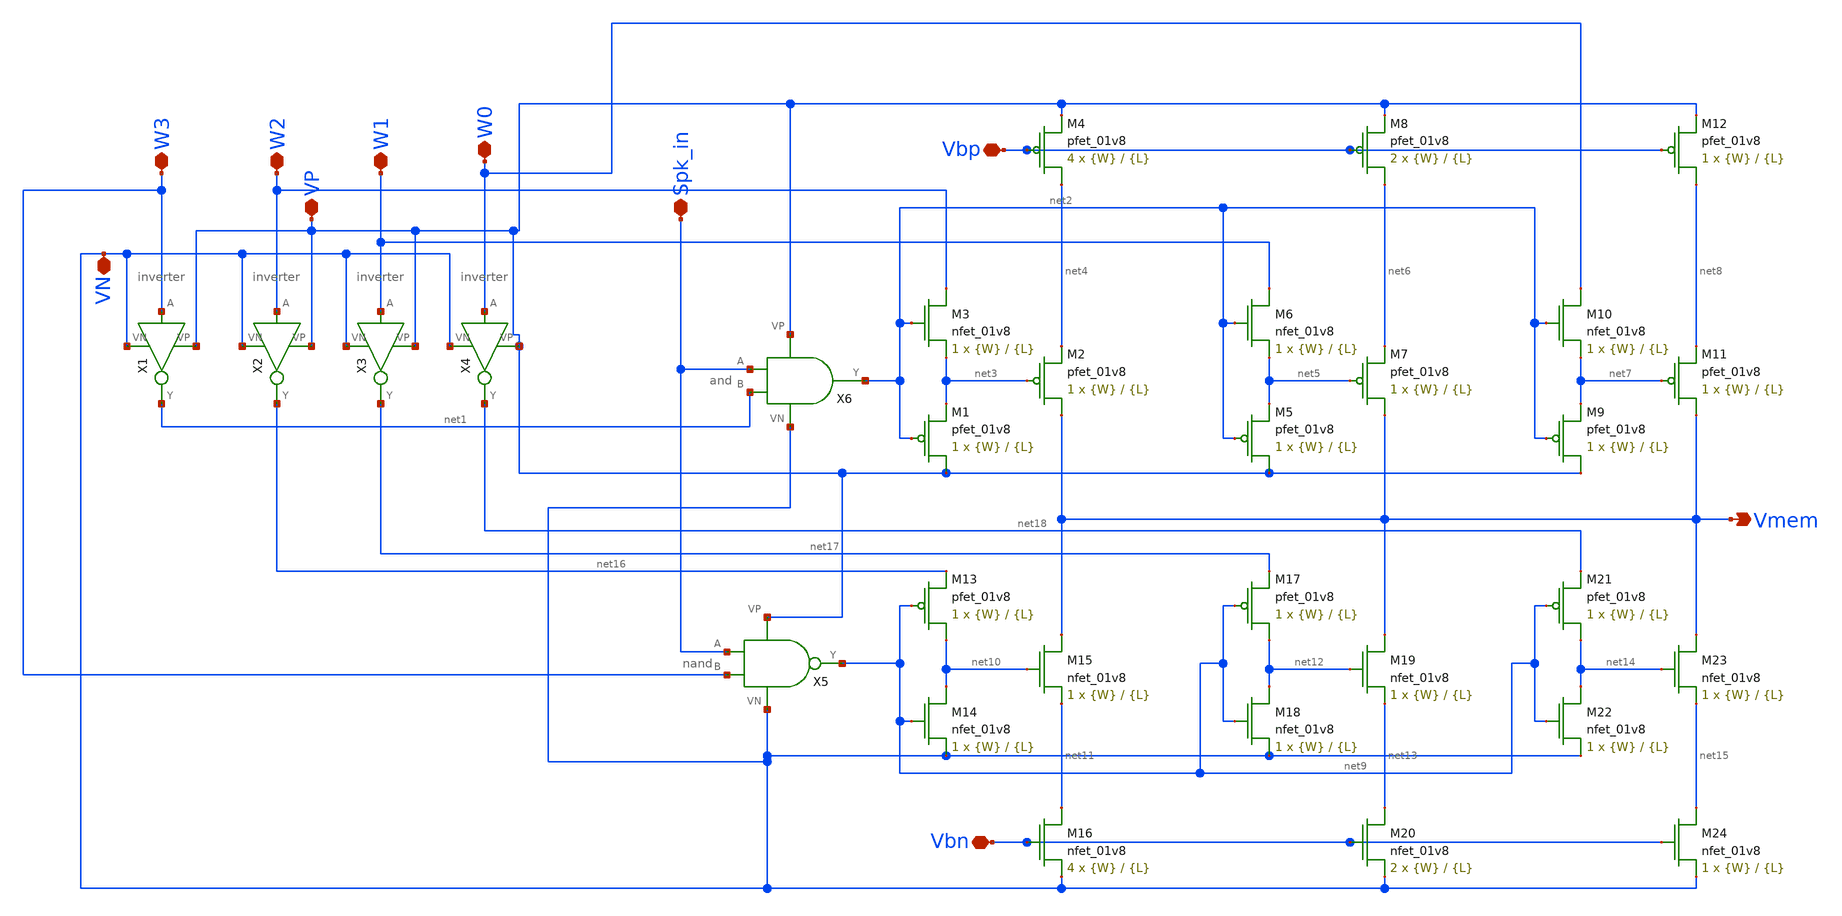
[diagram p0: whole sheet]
** sch_path: schematic/BECI_asghar_synapse.sch
**.subckt BECI_asghar_synapse W3 W2 W1 W0 Vbp Vbn VP VN Spk_in Vmem
*.iopin W3
*.iopin W2
*.iopin W1
*.iopin W0
*.iopin Vbp
*.iopin Vbn
*.iopin VP
*.iopin VN
*.iopin Spk_in
*.opin Vmem
X1 W3 VN VP net1 inverter
X2 W2 VN VP net16 inverter
X3 W1 VN VP net17 inverter
X4 W0 VN VP net18 inverter
X5 Spk_in W3 net9 VP VN nand
X6 Spk_in net1 net2 VP VN and
XM1 VP net2 net3 VDD sky130_fd_pr__pfet_01v8 L={L} W={W} nf=1 ad='int((nf+1)/2) * W/nf * 0.29' as='int((nf+2)/2) * W/nf * 0.29'
+ pd='2*int((nf+1)/2) * (W/nf + 0.29)' ps='2*int((nf+2)/2) * (W/nf + 0.29)' nrd='0.29 / W' nrs='0.29 / W'
+ sa=0 sb=0 sd=0 mult=1 m=1
XM3 W2 net2 net3 GND sky130_fd_pr__nfet_01v8 L={L} W={W} nf=1 ad='int((nf+1)/2) * W/nf * 0.29' as='int((nf+2)/2) * W/nf * 0.29'
+ pd='2*int((nf+1)/2) * (W/nf + 0.29)' ps='2*int((nf+2)/2) * (W/nf + 0.29)' nrd='0.29 / W' nrs='0.29 / W'
+ sa=0 sb=0 sd=0 mult=1 m=1
XM2 Vmem net3 net4 VDD sky130_fd_pr__pfet_01v8 L={L} W={W} nf=1 ad='int((nf+1)/2) * W/nf * 0.29' as='int((nf+2)/2) * W/nf * 0.29'
+ pd='2*int((nf+1)/2) * (W/nf + 0.29)' ps='2*int((nf+2)/2) * (W/nf + 0.29)' nrd='0.29 / W' nrs='0.29 / W'
+ sa=0 sb=0 sd=0 mult=1 m=1
XM4 net4 Vbp VP VDD sky130_fd_pr__pfet_01v8 L={L} W={W} nf=1 ad='int((nf+1)/2) * W/nf * 0.29' as='int((nf+2)/2) * W/nf * 0.29'
+ pd='2*int((nf+1)/2) * (W/nf + 0.29)' ps='2*int((nf+2)/2) * (W/nf + 0.29)' nrd='0.29 / W' nrs='0.29 / W'
+ sa=0 sb=0 sd=0 mult=4 m=4
XM5 VP net2 net5 VDD sky130_fd_pr__pfet_01v8 L={L} W={W} nf=1 ad='int((nf+1)/2) * W/nf * 0.29' as='int((nf+2)/2) * W/nf * 0.29'
+ pd='2*int((nf+1)/2) * (W/nf + 0.29)' ps='2*int((nf+2)/2) * (W/nf + 0.29)' nrd='0.29 / W' nrs='0.29 / W'
+ sa=0 sb=0 sd=0 mult=1 m=1
XM6 W1 net2 net5 GND sky130_fd_pr__nfet_01v8 L={L} W={W} nf=1 ad='int((nf+1)/2) * W/nf * 0.29' as='int((nf+2)/2) * W/nf * 0.29'
+ pd='2*int((nf+1)/2) * (W/nf + 0.29)' ps='2*int((nf+2)/2) * (W/nf + 0.29)' nrd='0.29 / W' nrs='0.29 / W'
+ sa=0 sb=0 sd=0 mult=1 m=1
XM7 Vmem net5 net6 VDD sky130_fd_pr__pfet_01v8 L={L} W={W} nf=1 ad='int((nf+1)/2) * W/nf * 0.29' as='int((nf+2)/2) * W/nf * 0.29'
+ pd='2*int((nf+1)/2) * (W/nf + 0.29)' ps='2*int((nf+2)/2) * (W/nf + 0.29)' nrd='0.29 / W' nrs='0.29 / W'
+ sa=0 sb=0 sd=0 mult=1 m=1
XM8 net6 Vbp VP VDD sky130_fd_pr__pfet_01v8 L={L} W={W} nf=1 ad='int((nf+1)/2) * W/nf * 0.29' as='int((nf+2)/2) * W/nf * 0.29'
+ pd='2*int((nf+1)/2) * (W/nf + 0.29)' ps='2*int((nf+2)/2) * (W/nf + 0.29)' nrd='0.29 / W' nrs='0.29 / W'
+ sa=0 sb=0 sd=0 mult=2 m=2
XM9 VP net2 net7 VDD sky130_fd_pr__pfet_01v8 L={L} W={W} nf=1 ad='int((nf+1)/2) * W/nf * 0.29' as='int((nf+2)/2) * W/nf * 0.29'
+ pd='2*int((nf+1)/2) * (W/nf + 0.29)' ps='2*int((nf+2)/2) * (W/nf + 0.29)' nrd='0.29 / W' nrs='0.29 / W'
+ sa=0 sb=0 sd=0 mult=1 m=1
XM10 W0 net2 net7 GND sky130_fd_pr__nfet_01v8 L={L} W={W} nf=1 ad='int((nf+1)/2) * W/nf * 0.29' as='int((nf+2)/2) * W/nf * 0.29'
+ pd='2*int((nf+1)/2) * (W/nf + 0.29)' ps='2*int((nf+2)/2) * (W/nf + 0.29)' nrd='0.29 / W' nrs='0.29 / W'
+ sa=0 sb=0 sd=0 mult=1 m=1
XM11 Vmem net7 net8 VDD sky130_fd_pr__pfet_01v8 L={L} W={W} nf=1 ad='int((nf+1)/2) * W/nf * 0.29' as='int((nf+2)/2) * W/nf * 0.29'
+ pd='2*int((nf+1)/2) * (W/nf + 0.29)' ps='2*int((nf+2)/2) * (W/nf + 0.29)' nrd='0.29 / W' nrs='0.29 / W'
+ sa=0 sb=0 sd=0 mult=1 m=1
XM12 net8 Vbp VP VDD sky130_fd_pr__pfet_01v8 L={L} W={W} nf=1 ad='int((nf+1)/2) * W/nf * 0.29' as='int((nf+2)/2) * W/nf * 0.29'
+ pd='2*int((nf+1)/2) * (W/nf + 0.29)' ps='2*int((nf+2)/2) * (W/nf + 0.29)' nrd='0.29 / W' nrs='0.29 / W'
+ sa=0 sb=0 sd=0 mult=1 m=1
XM13 net10 net9 net16 VDD sky130_fd_pr__pfet_01v8 L={L} W={W} nf=1 ad='int((nf+1)/2) * W/nf * 0.29' as='int((nf+2)/2) * W/nf * 0.29'
+ pd='2*int((nf+1)/2) * (W/nf + 0.29)' ps='2*int((nf+2)/2) * (W/nf + 0.29)' nrd='0.29 / W' nrs='0.29 / W'
+ sa=0 sb=0 sd=0 mult=1 m=1
XM14 net10 net9 VN GND sky130_fd_pr__nfet_01v8 L={L} W={W} nf=1 ad='int((nf+1)/2) * W/nf * 0.29' as='int((nf+2)/2) * W/nf * 0.29'
+ pd='2*int((nf+1)/2) * (W/nf + 0.29)' ps='2*int((nf+2)/2) * (W/nf + 0.29)' nrd='0.29 / W' nrs='0.29 / W'
+ sa=0 sb=0 sd=0 mult=1 m=1
XM15 Vmem net10 net11 GND sky130_fd_pr__nfet_01v8 L={L} W={W} nf=1 ad='int((nf+1)/2) * W/nf * 0.29' as='int((nf+2)/2) * W/nf * 0.29'
+ pd='2*int((nf+1)/2) * (W/nf + 0.29)' ps='2*int((nf+2)/2) * (W/nf + 0.29)' nrd='0.29 / W' nrs='0.29 / W'
+ sa=0 sb=0 sd=0 mult=1 m=1
XM16 net11 Vbn VN GND sky130_fd_pr__nfet_01v8 L={L} W={W} nf=1 ad='int((nf+1)/2) * W/nf * 0.29' as='int((nf+2)/2) * W/nf * 0.29'
+ pd='2*int((nf+1)/2) * (W/nf + 0.29)' ps='2*int((nf+2)/2) * (W/nf + 0.29)' nrd='0.29 / W' nrs='0.29 / W'
+ sa=0 sb=0 sd=0 mult=4 m=4
XM17 net12 net9 net17 VDD sky130_fd_pr__pfet_01v8 L={L} W={W} nf=1 ad='int((nf+1)/2) * W/nf * 0.29' as='int((nf+2)/2) * W/nf * 0.29'
+ pd='2*int((nf+1)/2) * (W/nf + 0.29)' ps='2*int((nf+2)/2) * (W/nf + 0.29)' nrd='0.29 / W' nrs='0.29 / W'
+ sa=0 sb=0 sd=0 mult=1 m=1
XM18 net12 net9 VN GND sky130_fd_pr__nfet_01v8 L={L} W={W} nf=1 ad='int((nf+1)/2) * W/nf * 0.29' as='int((nf+2)/2) * W/nf * 0.29'
+ pd='2*int((nf+1)/2) * (W/nf + 0.29)' ps='2*int((nf+2)/2) * (W/nf + 0.29)' nrd='0.29 / W' nrs='0.29 / W'
+ sa=0 sb=0 sd=0 mult=1 m=1
XM19 Vmem net12 net13 GND sky130_fd_pr__nfet_01v8 L={L} W={W} nf=1 ad='int((nf+1)/2) * W/nf * 0.29' as='int((nf+2)/2) * W/nf * 0.29'
+ pd='2*int((nf+1)/2) * (W/nf + 0.29)' ps='2*int((nf+2)/2) * (W/nf + 0.29)' nrd='0.29 / W' nrs='0.29 / W'
+ sa=0 sb=0 sd=0 mult=1 m=1
XM20 net13 Vbn VN GND sky130_fd_pr__nfet_01v8 L={L} W={W} nf=1 ad='int((nf+1)/2) * W/nf * 0.29' as='int((nf+2)/2) * W/nf * 0.29'
+ pd='2*int((nf+1)/2) * (W/nf + 0.29)' ps='2*int((nf+2)/2) * (W/nf + 0.29)' nrd='0.29 / W' nrs='0.29 / W'
+ sa=0 sb=0 sd=0 mult=2 m=2
XM21 net14 net9 net18 VDD sky130_fd_pr__pfet_01v8 L={L} W={W} nf=1 ad='int((nf+1)/2) * W/nf * 0.29' as='int((nf+2)/2) * W/nf * 0.29'
+ pd='2*int((nf+1)/2) * (W/nf + 0.29)' ps='2*int((nf+2)/2) * (W/nf + 0.29)' nrd='0.29 / W' nrs='0.29 / W'
+ sa=0 sb=0 sd=0 mult=1 m=1
XM22 net14 net9 VN GND sky130_fd_pr__nfet_01v8 L={L} W={W} nf=1 ad='int((nf+1)/2) * W/nf * 0.29' as='int((nf+2)/2) * W/nf * 0.29'
+ pd='2*int((nf+1)/2) * (W/nf + 0.29)' ps='2*int((nf+2)/2) * (W/nf + 0.29)' nrd='0.29 / W' nrs='0.29 / W'
+ sa=0 sb=0 sd=0 mult=1 m=1
XM23 Vmem net14 net15 GND sky130_fd_pr__nfet_01v8 L={L} W={W} nf=1 ad='int((nf+1)/2) * W/nf * 0.29' as='int((nf+2)/2) * W/nf * 0.29'
+ pd='2*int((nf+1)/2) * (W/nf + 0.29)' ps='2*int((nf+2)/2) * (W/nf + 0.29)' nrd='0.29 / W' nrs='0.29 / W'
+ sa=0 sb=0 sd=0 mult=1 m=1
XM24 net15 Vbn VN GND sky130_fd_pr__nfet_01v8 L={L} W={W} nf=1 ad='int((nf+1)/2) * W/nf * 0.29' as='int((nf+2)/2) * W/nf * 0.29'
+ pd='2*int((nf+1)/2) * (W/nf + 0.29)' ps='2*int((nf+2)/2) * (W/nf + 0.29)' nrd='0.29 / W' nrs='0.29 / W'
+ sa=0 sb=0 sd=0 mult=1 m=1
**.ends
.end
